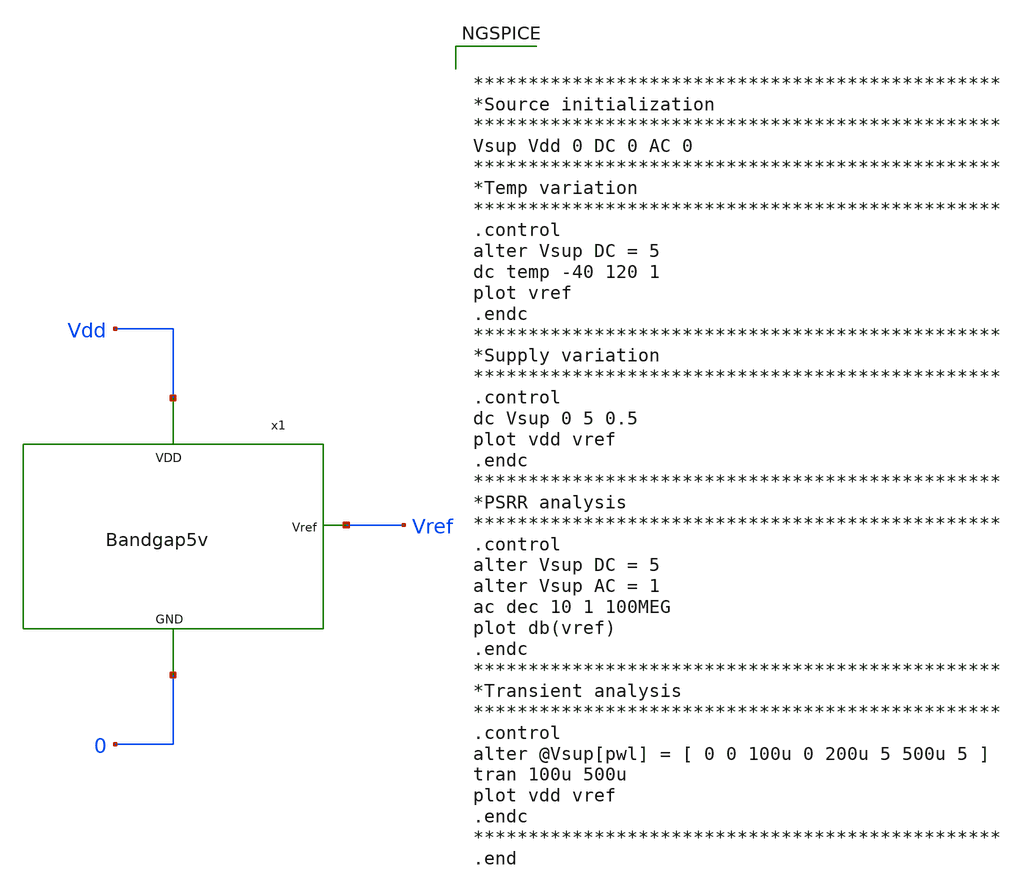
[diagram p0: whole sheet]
** sch_path: Analog_Blocks/Bandgap/Testbench/Bandgap5v_TB.sch
**.subckt Bandgap5v_TB
x1 Vref Vdd 0 Bandgap5v
**** begin user architecture code


************************************************
*Source initialization
************************************************
Vsup Vdd 0 DC 0 AC 0
************************************************
*Temp variation
************************************************
.control
alter Vsup DC = 5
dc temp -40 120 1
plot vref
.endc
************************************************
*Supply variation
************************************************
.control
dc Vsup 0 5 0.5
plot vdd vref
.endc
************************************************
*PSRR analysis
************************************************
.control
alter Vsup DC = 5
alter Vsup AC = 1
ac dec 10 1 100MEG
plot db(vref)
.endc
************************************************
*Transient analysis
************************************************
.control
alter @Vsup[pwl] = [ 0 0 100u 0 200u 5 500u 5 ]
tran 100u 500u
plot vdd vref
.endc
************************************************
.end



.include $::SKYWATER_MODELS/cells/nfet_01v8/sky130_fd_pr__nfet_01v8__tt.corner.spice
.include $::SKYWATER_MODELS/cells/nfet_01v8_lvt/sky130_fd_pr__nfet_01v8_lvt__tt.corner.spice
.include $::SKYWATER_MODELS/cells/pfet_01v8/sky130_fd_pr__pfet_01v8__tt.corner.spice
.include $::SKYWATER_MODELS/cells/nfet_03v3_nvt/sky130_fd_pr__nfet_03v3_nvt__tt.corner.spice
.include $::SKYWATER_MODELS/cells/nfet_05v0_nvt/sky130_fd_pr__nfet_05v0_nvt__tt.corner.spice
.include $::SKYWATER_MODELS/cells/esd_nfet_01v8/sky130_fd_pr__esd_nfet_01v8__tt.corner.spice
.include $::SKYWATER_MODELS/cells/pfet_01v8_lvt/sky130_fd_pr__pfet_01v8_lvt__tt.corner.spice
.include $::SKYWATER_MODELS/cells/pfet_01v8_hvt/sky130_fd_pr__pfet_01v8_hvt__tt.corner.spice
.include $::SKYWATER_MODELS/cells/esd_pfet_g5v0d10v5/sky130_fd_pr__esd_pfet_g5v0d10v5__tt.corner.spice
.include $::SKYWATER_MODELS/cells/pfet_g5v0d10v5/sky130_fd_pr__pfet_g5v0d10v5__tt.corner.spice
.include $::SKYWATER_MODELS/cells/pfet_g5v0d16v0/sky130_fd_pr__pfet_g5v0d16v0__tt.corner.spice
.include $::SKYWATER_MODELS/cells/nfet_g5v0d10v5/sky130_fd_pr__nfet_g5v0d10v5__tt.corner.spice
.include $::SKYWATER_MODELS/cells/nfet_g5v0d16v0/sky130_fd_pr__nfet_g5v0d16v0__tt_discrete.corner.spice
.include $::SKYWATER_MODELS/cells/esd_nfet_g5v0d10v5/sky130_fd_pr__esd_nfet_g5v0d10v5__tt.corner.spice
.include $::SKYWATER_MODELS/models/corners/tt/nonfet.spice
* Mismatch parameters
.include $::SKYWATER_MODELS/cells/nfet_01v8/sky130_fd_pr__nfet_01v8__mismatch.corner.spice
.include $::SKYWATER_MODELS/cells/pfet_01v8/sky130_fd_pr__pfet_01v8__mismatch.corner.spice
.include $::SKYWATER_MODELS/cells/nfet_01v8_lvt/sky130_fd_pr__nfet_01v8_lvt__mismatch.corner.spice
.include $::SKYWATER_MODELS/cells/pfet_01v8_lvt/sky130_fd_pr__pfet_01v8_lvt__mismatch.corner.spice
.include $::SKYWATER_MODELS/cells/pfet_01v8_hvt/sky130_fd_pr__pfet_01v8_hvt__mismatch.corner.spice
.include $::SKYWATER_MODELS/cells/nfet_g5v0d10v5/sky130_fd_pr__nfet_g5v0d10v5__mismatch.corner.spice
.include $::SKYWATER_MODELS/cells/pfet_g5v0d10v5/sky130_fd_pr__pfet_g5v0d10v5__mismatch.corner.spice
.include $::SKYWATER_MODELS/cells/nfet_05v0_nvt/sky130_fd_pr__nfet_05v0_nvt__mismatch.corner.spice
.include $::SKYWATER_MODELS/cells/nfet_03v3_nvt/sky130_fd_pr__nfet_03v3_nvt__mismatch.corner.spice
* Resistor$::SKYWATER_MODELS/Capacitor
.include $::SKYWATER_MODELS/models/r+c/res_typical__cap_typical.spice
.include $::SKYWATER_MODELS/models/r+c/res_typical__cap_typical__lin.spice
* Special cells
.include $::SKYWATER_MODELS/models/corners/tt/specialized_cells.spice
* All models
.include $::SKYWATER_MODELS/models/all.spice
* Corner
.include $::SKYWATER_MODELS/models/corners/tt/rf.spice

**** end user architecture code
**.ends

* expanding   symbol:
*+  /home/eslam/Analog_Design/Analog_Blocks/Bandgap/Schematics/BGR5v/Bandgap5v.sym # of pins=3
** sym_path: Analog_Blocks/Bandgap/Schematics/BGR5v/Bandgap5v.sym
** sch_path: Analog_Blocks/Bandgap/Schematics/BGR5v/Bandgap5v.sch
.subckt Bandgap5v Vref VDD GND
*.ipin VDD
*.ipin GND
*.opin Vref
XQ1 GND GND net3 sky130_fd_pr__pnp_05v5_W0p68L0p68 m=1
XQ2 GND GND net1 sky130_fd_pr__pnp_05v5_W0p68L0p68 m=1
XQ3 GND GND net1 sky130_fd_pr__pnp_05v5_W0p68L0p68 m=1
XQ4 GND GND net1 sky130_fd_pr__pnp_05v5_W0p68L0p68 m=1
XQ5 GND GND net1 sky130_fd_pr__pnp_05v5_W0p68L0p68 m=1
XQ6 GND GND net1 sky130_fd_pr__pnp_05v5_W0p68L0p68 m=1
XQ7 GND GND net1 sky130_fd_pr__pnp_05v5_W0p68L0p68 m=1
XQ8 GND GND net1 sky130_fd_pr__pnp_05v5_W0p68L0p68 m=1
XQ9 GND GND net1 sky130_fd_pr__pnp_05v5_W0p68L0p68 m=1
XM2 net4 net5 VDD VDD sky130_fd_pr__pfet_g5v0d10v5 L=1 W=10 nf=1 ad='int((nf+1)/2) * W/nf * 0.29' as='int((nf+2)/2) * W/nf * 0.29'
+ pd='2*int((nf+1)/2) * (W/nf + 0.29)' ps='2*int((nf+2)/2) * (W/nf + 0.29)' nrd='0.29 / W' nrs='0.29 / W'
+ sa=0 sb=0 sd=0 mult=1 m=1
XM3 net3 net4 VDD VDD sky130_fd_pr__pfet_g5v0d10v5 L=1 W=10 nf=1 ad='int((nf+1)/2) * W/nf * 0.29' as='int((nf+2)/2) * W/nf * 0.29'
+ pd='2*int((nf+1)/2) * (W/nf + 0.29)' ps='2*int((nf+2)/2) * (W/nf + 0.29)' nrd='0.29 / W' nrs='0.29 / W'
+ sa=0 sb=0 sd=0 mult=1 m=1
XM1 net4 net5 GND GND sky130_fd_pr__nfet_g5v0d10v5 L=40 W=1 nf=1 ad='int((nf+1)/2) * W/nf * 0.29' as='int((nf+2)/2) * W/nf * 0.29'
+ pd='2*int((nf+1)/2) * (W/nf + 0.29)' ps='2*int((nf+2)/2) * (W/nf + 0.29)' nrd='0.29 / W' nrs='0.29 / W'
+ sa=0 sb=0 sd=0 mult=1 m=1
XR1 net2 Vref GND sky130_fd_pr__res_high_po W=1 L=6 mult=1 m=1
XR3 net3 Vref GND sky130_fd_pr__res_high_po W=1 L=6 mult=1 m=1
XR2 net1 net2 GND sky130_fd_pr__res_high_po W=1 L=2.6 mult=1 m=1
x1 VDD net3 net2 Vref net5 GND Bandgap5v_OTA
.ends


* expanding   symbol:
*+  /home/eslam/Analog_Design/Analog_Blocks/Bandgap/Schematics/BGR5v/Bandgap5v_OTA.sym # of pins=6
** sym_path: LDO/Schematic/Bandgap5v_OTA.sym
** sch_path: LDO/Schematic/Bandgap5v_OTA.sch
.subckt Bandgap5v_OTA Vdd Vn Vp Ibias Vhigh Gnd
*.opin Ibias
*.ipin Vhigh
*.ipin Vdd
*.ipin Gnd
*.ipin Vn
*.ipin Vp
XM6 Ibias Vhigh Vdd Vdd sky130_fd_pr__pfet_g5v0d10v5 L=1 W=10 nf=1 ad='int((nf+1)/2) * W/nf * 0.29' as='int((nf+2)/2) * W/nf * 0.29'
+ pd='2*int((nf+1)/2) * (W/nf + 0.29)' ps='2*int((nf+2)/2) * (W/nf + 0.29)' nrd='0.29 / W' nrs='0.29 / W'
+ sa=0 sb=0 sd=0 mult=1 m=1
XM5 net3 Vhigh Vdd Vdd sky130_fd_pr__pfet_g5v0d10v5 L=1 W=10 nf=1 ad='int((nf+1)/2) * W/nf * 0.29' as='int((nf+2)/2) * W/nf * 0.29'
+ pd='2*int((nf+1)/2) * (W/nf + 0.29)' ps='2*int((nf+2)/2) * (W/nf + 0.29)' nrd='0.29 / W' nrs='0.29 / W'
+ sa=0 sb=0 sd=0 mult=1 m=1
XM7 Vhigh Vhigh Vdd Vdd sky130_fd_pr__pfet_g5v0d10v5 L=1 W=54 nf=1 ad='int((nf+1)/2) * W/nf * 0.29' as='int((nf+2)/2) * W/nf * 0.29'
+ pd='2*int((nf+1)/2) * (W/nf + 0.29)' ps='2*int((nf+2)/2) * (W/nf + 0.29)' nrd='0.29 / W' nrs='0.29 / W'
+ sa=0 sb=0 sd=0 mult=1 m=1
XM2 net1 Vp net3 Vdd sky130_fd_pr__pfet_g5v0d10v5 L=1 W=30 nf=1 ad='int((nf+1)/2) * W/nf * 0.29' as='int((nf+2)/2) * W/nf * 0.29'
+ pd='2*int((nf+1)/2) * (W/nf + 0.29)' ps='2*int((nf+2)/2) * (W/nf + 0.29)' nrd='0.29 / W' nrs='0.29 / W'
+ sa=0 sb=0 sd=0 mult=1 m=1
XM1 net2 Vn net3 Vdd sky130_fd_pr__pfet_g5v0d10v5 L=1 W=30 nf=1 ad='int((nf+1)/2) * W/nf * 0.29' as='int((nf+2)/2) * W/nf * 0.29'
+ pd='2*int((nf+1)/2) * (W/nf + 0.29)' ps='2*int((nf+2)/2) * (W/nf + 0.29)' nrd='0.29 / W' nrs='0.29 / W'
+ sa=0 sb=0 sd=0 mult=1 m=1
XM8 Vhigh net1 Gnd Gnd sky130_fd_pr__nfet_g5v0d10v5 L=0.5 W=75 nf=1 ad='int((nf+1)/2) * W/nf * 0.29'
+ as='int((nf+2)/2) * W/nf * 0.29' pd='2*int((nf+1)/2) * (W/nf + 0.29)' ps='2*int((nf+2)/2) * (W/nf + 0.29)'
+ nrd='0.29 / W' nrs='0.29 / W' sa=0 sb=0 sd=0 mult=1 m=1
XM4 net1 net2 Gnd Gnd sky130_fd_pr__nfet_g5v0d10v5 L=0.5 W=7.5 nf=1 ad='int((nf+1)/2) * W/nf * 0.29'
+ as='int((nf+2)/2) * W/nf * 0.29' pd='2*int((nf+1)/2) * (W/nf + 0.29)' ps='2*int((nf+2)/2) * (W/nf + 0.29)'
+ nrd='0.29 / W' nrs='0.29 / W' sa=0 sb=0 sd=0 mult=1 m=1
XM3 net2 net2 Gnd Gnd sky130_fd_pr__nfet_g5v0d10v5 L=0.5 W=7.5 nf=1 ad='int((nf+1)/2) * W/nf * 0.29'
+ as='int((nf+2)/2) * W/nf * 0.29' pd='2*int((nf+1)/2) * (W/nf + 0.29)' ps='2*int((nf+2)/2) * (W/nf + 0.29)'
+ nrd='0.29 / W' nrs='0.29 / W' sa=0 sb=0 sd=0 mult=1 m=1
XC1 net1 Vhigh sky130_fd_pr__cap_mim_m3_2 W=1 L=1 MF=1 m=1
.ends

.end
